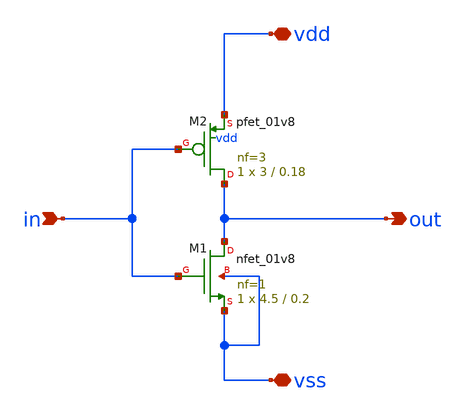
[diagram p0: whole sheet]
** sch_path: inverter_new/xschem/inverter_new.sch
**.subckt inverter_new in vdd vss out
*.ipin in
*.iopin vdd
*.iopin vss
*.opin out
XM2 out in vdd vdd sky130_fd_pr__pfet_01v8 L=0.18 W=3 nf=3 ad='int((nf+1)/2) * W/nf * 0.29' as='int((nf+2)/2) * W/nf * 0.29'
+ pd='2*int((nf+1)/2) * (W/nf + 0.29)' ps='2*int((nf+2)/2) * (W/nf + 0.29)' nrd='0.29 / W' nrs='0.29 / W'
+ sa=0 sb=0 sd=0 mult=1 m=1
XM1 out in vss vss sky130_fd_pr__nfet_01v8 L=0.2 W=4.5 nf=1 ad='int((nf+1)/2) * W/nf * 0.29' as='int((nf+2)/2) * W/nf * 0.29'
+ pd='2*int((nf+1)/2) * (W/nf + 0.29)' ps='2*int((nf+2)/2) * (W/nf + 0.29)' nrd='0.29 / W' nrs='0.29 / W'
+ sa=0 sb=0 sd=0 mult=1 m=1
**.ends
.end
